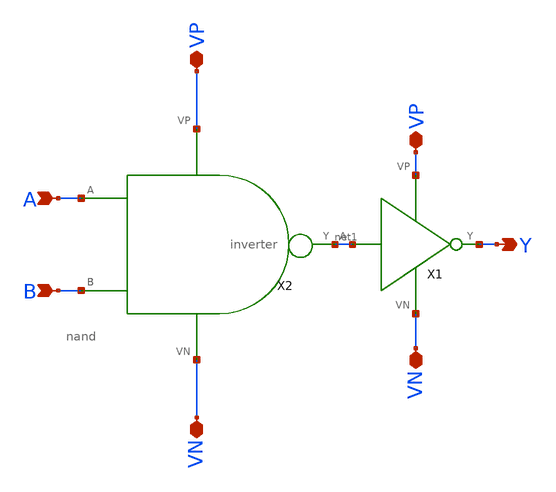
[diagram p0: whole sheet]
** sch_path: Miniproject 1/2_input_and.sch
**.subckt 2_input_and A B VP VP VN Y VN
*.ipin A
*.ipin B
*.iopin VP
*.iopin VP
*.iopin VN
*.opin Y
*.iopin VN
X1 net1 Y VP VN inverter
X2 A B net1 VP VN nand
**.ends

* expanding   symbol:  /home/madvlsi/Documents/inverter_tutorial/inverter.sym # of pins=4
** sym_path: Miniproject 1/inverter.sym
** sch_path: Miniproject 1/inverter.sch
.subckt inverter A Y VP VN
*.ipin A
*.iopin VP
*.iopin VN
*.opin Y
XM1 Y A VN VN sky130_fd_pr__nfet_01v8 L=0.15 W=1 nf=1 ad='int((nf+1)/2) * W/nf * 0.29' as='int((nf+2)/2) * W/nf * 0.29'
+ pd='2*int((nf+1)/2) * (W/nf + 0.29)' ps='2*int((nf+2)/2) * (W/nf + 0.29)' nrd='0.29 / W' nrs='0.29 / W'
+ sa=0 sb=0 sd=0 mult=1 m=1
XM2 Y A VP VP sky130_fd_pr__pfet_01v8 L=0.15 W=1 nf=1 ad='int((nf+1)/2) * W/nf * 0.29' as='int((nf+2)/2) * W/nf * 0.29'
+ pd='2*int((nf+1)/2) * (W/nf + 0.29)' ps='2*int((nf+2)/2) * (W/nf + 0.29)' nrd='0.29 / W' nrs='0.29 / W'
+ sa=0 sb=0 sd=0 mult=1 m=1
.ends


* expanding   symbol:  /home/madvlsi/Documents/inverter_tutorial/nand.sym # of pins=6
** sym_path: Miniproject 1/nand.sym
** sch_path: Miniproject 1/nand.sch
.subckt nand A B Y VP VN
*.iopin VP
*.iopin VP
*.opin Y
*.ipin A
*.ipin B
*.iopin VN
*.ipin A
*.ipin B
XM1 Y A VP VDD sky130_fd_pr__pfet_01v8 L=0.15 W=1 nf=1 ad='int((nf+1)/2) * W/nf * 0.29' as='int((nf+2)/2) * W/nf * 0.29'
+ pd='2*int((nf+1)/2) * (W/nf + 0.29)' ps='2*int((nf+2)/2) * (W/nf + 0.29)' nrd='0.29 / W' nrs='0.29 / W'
+ sa=0 sb=0 sd=0 mult=1 m=1
XM2 VP B Y VDD sky130_fd_pr__pfet_01v8 L=0.15 W=1 nf=1 ad='int((nf+1)/2) * W/nf * 0.29' as='int((nf+2)/2) * W/nf * 0.29'
+ pd='2*int((nf+1)/2) * (W/nf + 0.29)' ps='2*int((nf+2)/2) * (W/nf + 0.29)' nrd='0.29 / W' nrs='0.29 / W'
+ sa=0 sb=0 sd=0 mult=1 m=1
XM3 Y A net1 GND sky130_fd_pr__nfet_01v8 L=0.15 W=1 nf=1 ad='int((nf+1)/2) * W/nf * 0.29' as='int((nf+2)/2) * W/nf * 0.29'
+ pd='2*int((nf+1)/2) * (W/nf + 0.29)' ps='2*int((nf+2)/2) * (W/nf + 0.29)' nrd='0.29 / W' nrs='0.29 / W'
+ sa=0 sb=0 sd=0 mult=1 m=1
XM4 VN B net1 GND sky130_fd_pr__nfet_01v8 L=0.15 W=1 nf=1 ad='int((nf+1)/2) * W/nf * 0.29' as='int((nf+2)/2) * W/nf * 0.29'
+ pd='2*int((nf+1)/2) * (W/nf + 0.29)' ps='2*int((nf+2)/2) * (W/nf + 0.29)' nrd='0.29 / W' nrs='0.29 / W'
+ sa=0 sb=0 sd=0 mult=1 m=1
.ends

.end
